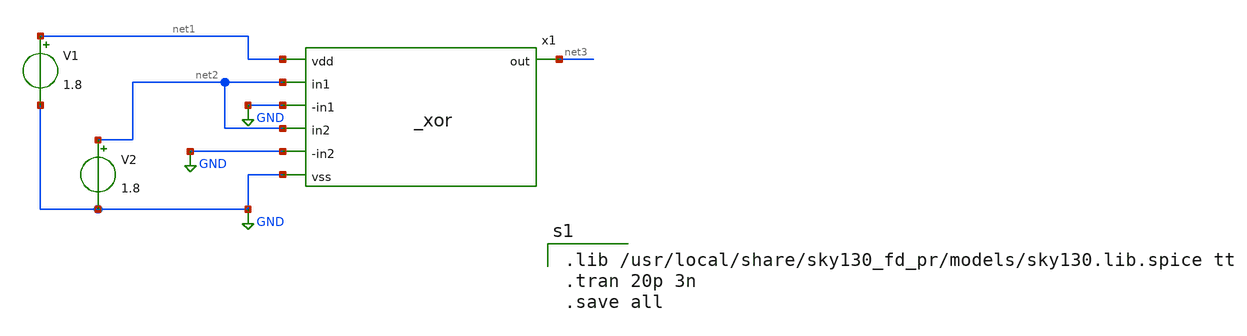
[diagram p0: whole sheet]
** sch_path: projects/carry_lookahead_adder/xschem/ports/test/true_table/_xor.sch
**.subckt _xor
V1 net1 GND 1.8
V2 net2 GND 1.8
x1 net1 net2 GND net3 net2 GND GND _xor
**** begin user architecture code

.lib /usr/local/share/sky130_fd_pr/models/sky130.lib.spice tt
.tran 20p 3n
.save all

**** end user architecture code
**.ends
.GLOBAL GND
.end
